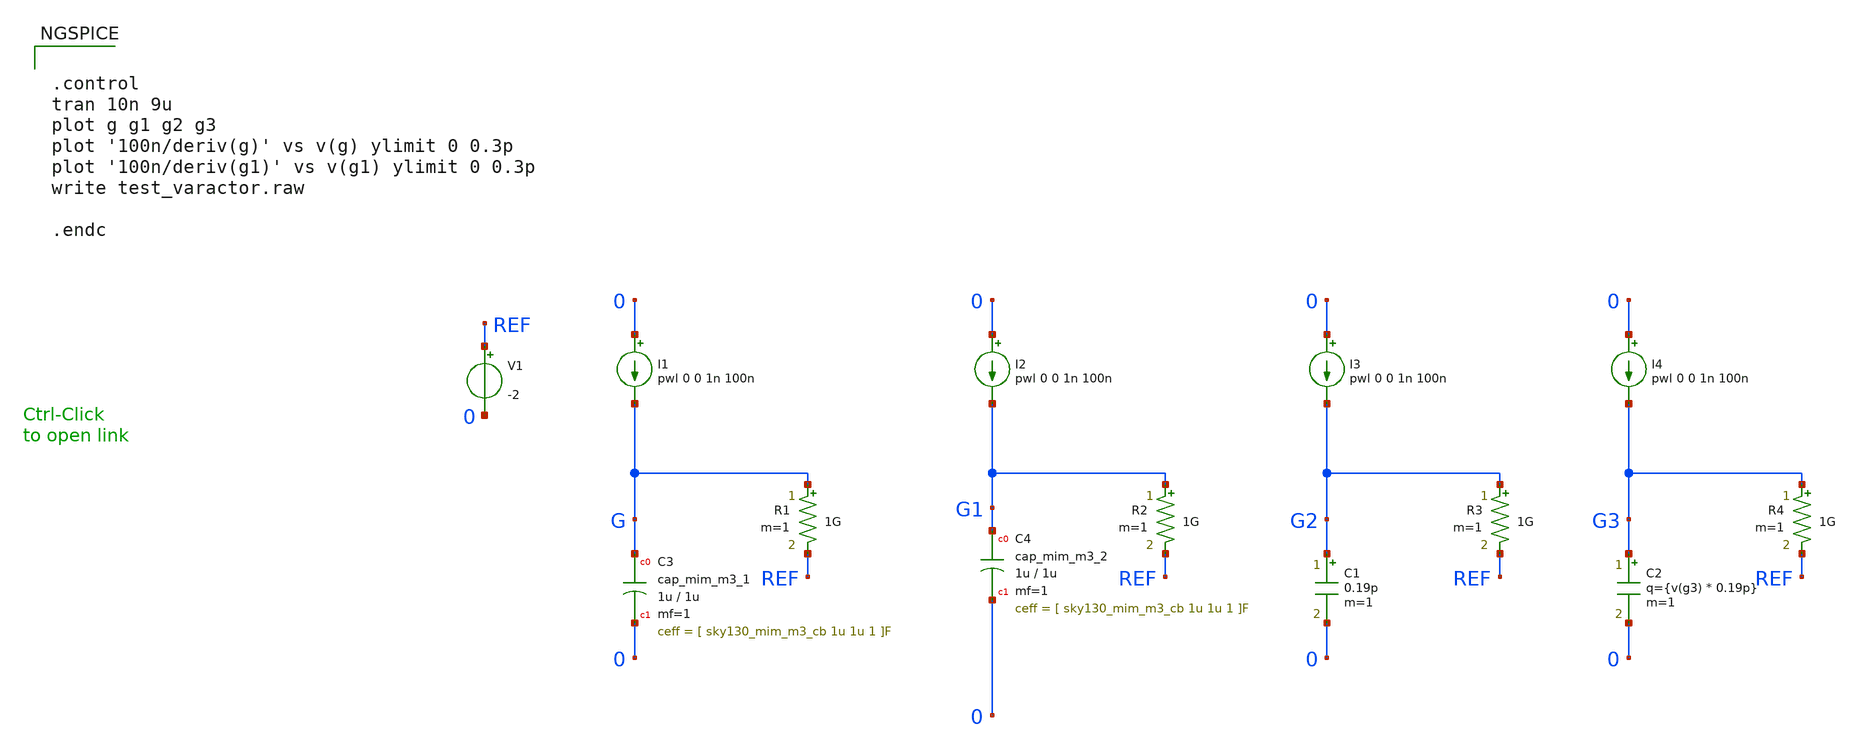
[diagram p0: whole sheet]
** sch_path: sky130_tests_ng/test_mim.sch
* Copyright 2020 Stefan Frederik Schippers
* Licensed under the Apache License, Version 2.0 (the "License");
* you may not use this file except in compliance with the License.
* You may obtain a copy of the License at
* https://www.apache.org/licenses/LICENSE-2.0
* Unless required by applicable law or agreed to in writing, software
* distributed under the License is distributed on an "AS IS" BASIS,
* WITHOUT WARRANTIES OR CONDITIONS OF ANY KIND, either express or implied.
* See the License for the specific language governing permissions and
* limitations under the License.
**.subckt test_mim
I1 0 G pwl 0 0 1n 100n
R1 G REF 1G m=1
I2 0 G1 pwl 0 0 1n 100n
R2 G1 REF 1G m=1
I3 0 G2 pwl 0 0 1n 100n
R3 G2 REF 1G m=1
C1 G2 0 0.19p m=1
V1 REF 0 -2
I4 0 G3 pwl 0 0 1n 100n
R4 G3 REF 1G m=1
C2 G3 0 q={v(g3) * 0.19p} m=1
XC4 G1 0 sky130_fd_pr__cap_mim_m3_2 w=1u l=1u mf=1
XC3 G 0 sky130_fd_pr__cap_mim_m3_1 w=1u l=1u mf=1 m=1
**** begin user architecture code


.control
tran 10n 9u
plot g g1 g2 g3
plot '100n/deriv(g)' vs v(g) ylimit 0 0.3p
plot '100n/deriv(g1)' vs v(g1) ylimit 0 0.3p
write test_varactor.raw

.endc



**** end user architecture code
**.ends
.end
